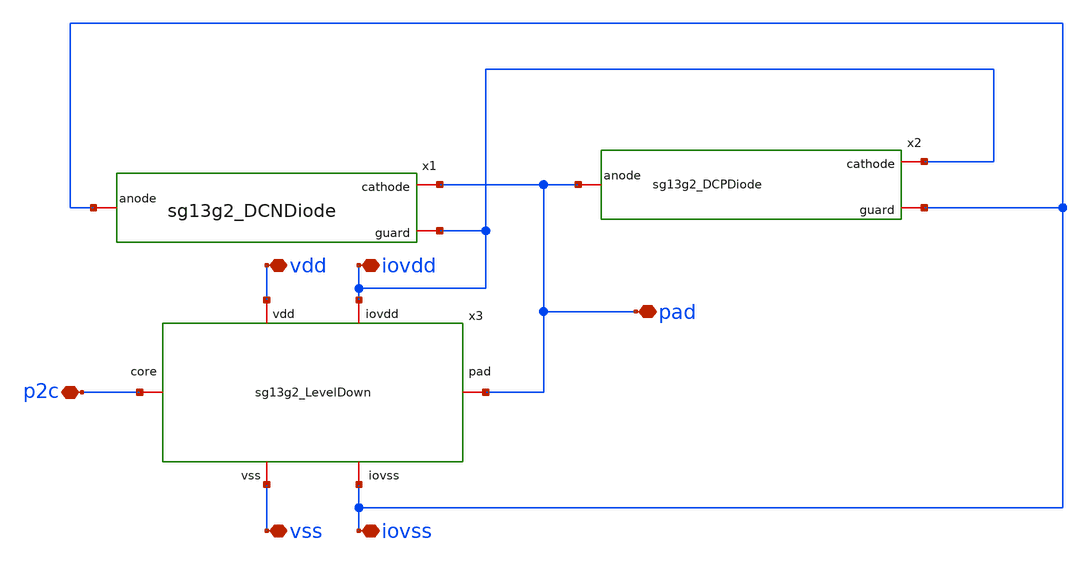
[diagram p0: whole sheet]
** sch_path: design/blocks-std/sg13g2_IOPadIn/schematic/sg13g2_IOPadIn.sch
**.subckt sg13g2_IOPadIn iovdd vdd vss iovss p2c pad
*.iopin iovdd
*.iopin vdd
*.iopin vss
*.iopin iovss
*.iopin p2c
*.iopin pad
x1 pad iovss iovdd sg13g2_DCNDiode
x2 iovdd pad iovss sg13g2_DCPDiode
x3 vdd iovdd p2c pad iovss vss sg13g2_LevelDown
**.ends
.end
